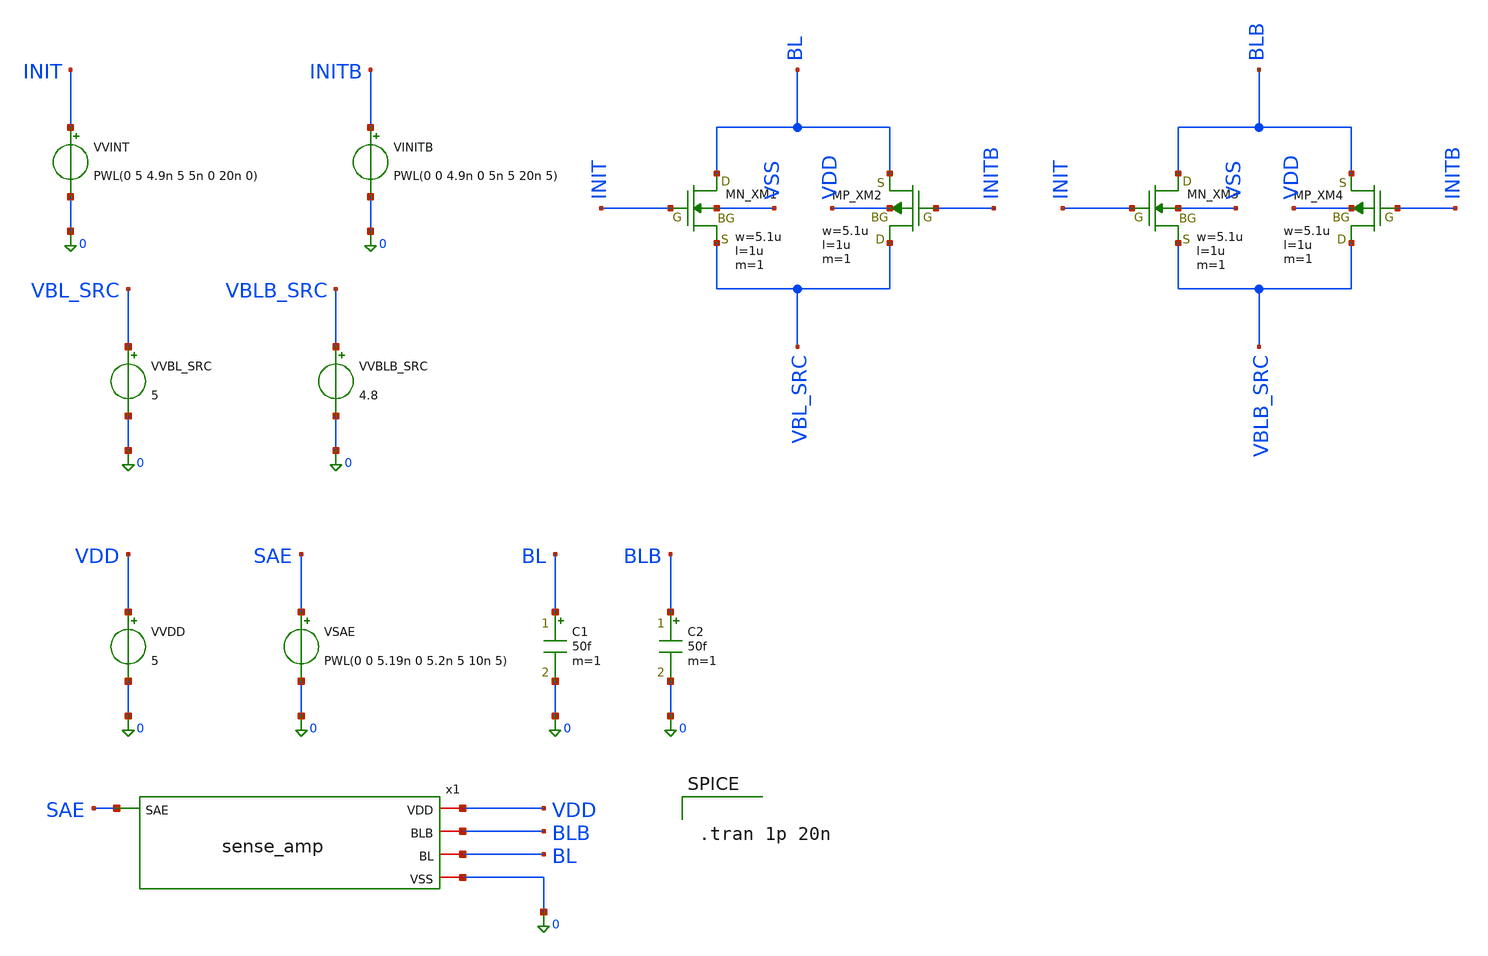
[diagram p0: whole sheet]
** sch_path: cell/tb_sense_amp_switch.sch
**.subckt tb_sense_amp_switch
x1 VDD BLB BL SAE 0 sense_amp
VVDD VDD 0 5
VSAE SAE 0 PWL(0 0 5.19n 0 5.2n 5 10n 5)
C1 BL 0 50f m=1
C2 BLB 0 50f m=1
VVBL_SRC VBL_SRC 0 5
VVBLB_SRC VBLB_SRC 0 4.8
XXM1 BL INIT VBL_SRC VSS NMOS w=5.1u l=1u nrd=0 nrs=0 m=1
XXM2 VBL_SRC INITB BL VDD PMOS w=5.1u l=1u nrd=0 nrs=0 m=1
XXM3 BLB INIT VBLB_SRC VSS NMOS w=5.1u l=1u nrd=0 nrs=0 m=1
XXM4 VBLB_SRC INITB BLB VDD PMOS w=5.1u l=1u nrd=0 nrs=0 m=1
VVINT INIT 0 PWL(0 5 4.9n 5 5n 0 20n 0)
VINITB INITB 0 PWL(0 0 4.9n 0 5n 5 20n 5)
**** begin user architecture code


.tran 1p 20n


 .include $::LIB/ip62_models
**** end user architecture code
**.ends
.end
